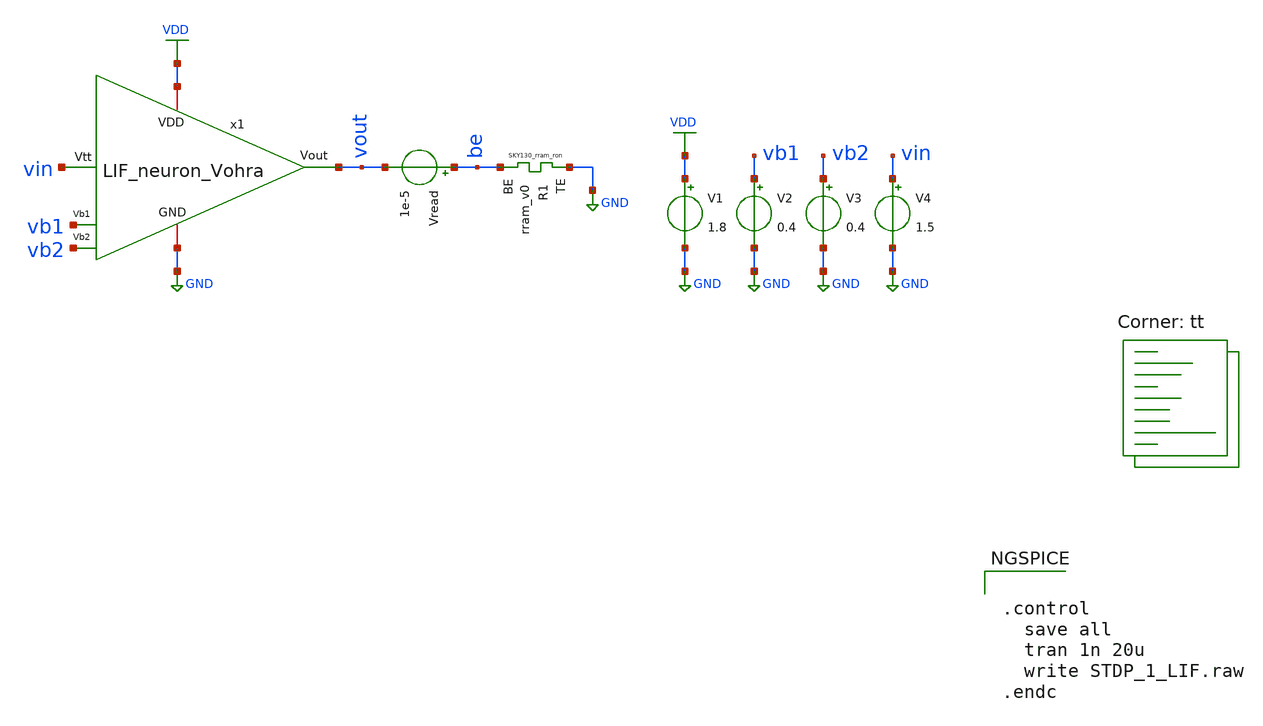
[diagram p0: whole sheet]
** sch_path: STDP/STDP_1_LIF.sch
**.subckt STDP_1_LIF
x1 VDD vout vb1 vin GND vb2 LIF_neuron_Vohra
V1 VDD GND 1.8
V4 vin GND 1.5
V2 vb1 GND 0.4
V3 vb2 GND 0.4
Vread be vout 1e-5
XR1 GND be rram_v0
**** begin user architecture code
.lib $::SKYWATER_MODELS/sky130.lib.spice tt

** opencircuitdesign pdks install
.inc $::SKYWATER_MODELS/rram_v0.spice



.control
  save all
  tran 1n 20u
  write STDP_1_LIF.raw
.endc


**** end user architecture code
**.ends

* expanding   symbol:  /home/ricardo/RATT_repos/Proyectos_xschem/LIF_neuron/LIF_neuron_Vohra.sym #
*+ of pins=6
** sym_path: LIF_neuron/LIF_neuron_Vohra.sym
** sch_path: LIF_neuron/LIF_neuron_Vohra.sch
.subckt LIF_neuron_Vohra VDD Vout Vb1 Vtt GND Vb2
*.ipin Vtt
*.iopin GND
*.ipin Vb1
*.ipin Vb2
*.iopin VDD
*.opin Vout
XM1 net3 Vtt GND GND sky130_fd_pr__nfet_01v8 L=1 W=0.6 nf=1 ad='int((nf+1)/2) * W/nf * 0.29' as='int((nf+2)/2) * W/nf * 0.29'
+ pd='2*int((nf+1)/2) * (W/nf + 0.29)' ps='2*int((nf+2)/2) * (W/nf + 0.29)' nrd='0.29 / W' nrs='0.29 / W'
+ sa=0 sb=0 sd=0 mult=1 m=1
XM3 net3 net3 VDD VDD sky130_fd_pr__pfet_01v8 L=1 W=0.6 nf=1 ad='int((nf+1)/2) * W/nf * 0.29' as='int((nf+2)/2) * W/nf * 0.29'
+ pd='2*int((nf+1)/2) * (W/nf + 0.29)' ps='2*int((nf+2)/2) * (W/nf + 0.29)' nrd='0.29 / W' nrs='0.29 / W'
+ sa=0 sb=0 sd=0 mult=1 m=1
XM13 net2 Vb1 GND GND sky130_fd_pr__nfet_01v8 L=0.5 W=5 nf=1 ad='int((nf+1)/2) * W/nf * 0.29' as='int((nf+2)/2) * W/nf * 0.29'
+ pd='2*int((nf+1)/2) * (W/nf + 0.29)' ps='2*int((nf+2)/2) * (W/nf + 0.29)' nrd='0.29 / W' nrs='0.29 / W'
+ sa=0 sb=0 sd=0 mult=1 m=1
XM12 rc net1 net2 GND sky130_fd_pr__nfet_01v8 L=1 W=1 nf=1 ad='int((nf+1)/2) * W/nf * 0.29' as='int((nf+2)/2) * W/nf * 0.29'
+ pd='2*int((nf+1)/2) * (W/nf + 0.29)' ps='2*int((nf+2)/2) * (W/nf + 0.29)' nrd='0.29 / W' nrs='0.29 / W'
+ sa=0 sb=0 sd=0 mult=1 m=1
XM11 rc net1 VDD VDD sky130_fd_pr__pfet_01v8 L=1 W=1 nf=1 ad='int((nf+1)/2) * W/nf * 0.29' as='int((nf+2)/2) * W/nf * 0.29'
+ pd='2*int((nf+1)/2) * (W/nf + 0.29)' ps='2*int((nf+2)/2) * (W/nf + 0.29)' nrd='0.29 / W' nrs='0.29 / W'
+ sa=0 sb=0 sd=0 mult=1 m=1
XC1 rc GND sky130_fd_pr__cap_mim_m3_1 W=21 L=1 MF=1 m=1
XM14 u rc GND GND sky130_fd_pr__nfet_01v8 L=4 W=1 nf=1 ad='int((nf+1)/2) * W/nf * 0.29' as='int((nf+2)/2) * W/nf * 0.29'
+ pd='2*int((nf+1)/2) * (W/nf + 0.29)' ps='2*int((nf+2)/2) * (W/nf + 0.29)' nrd='0.29 / W' nrs='0.29 / W'
+ sa=0 sb=0 sd=0 mult=1 m=1
XM4 u net3 VDD VDD sky130_fd_pr__pfet_01v8 L=1 W=1 nf=1 ad='int((nf+1)/2) * W/nf * 0.29' as='int((nf+2)/2) * W/nf * 0.29'
+ pd='2*int((nf+1)/2) * (W/nf + 0.29)' ps='2*int((nf+2)/2) * (W/nf + 0.29)' nrd='0.29 / W' nrs='0.29 / W'
+ sa=0 sb=0 sd=0 mult=1 m=1
XC2 u GND sky130_fd_pr__cap_mim_m3_1 W=10 L=1 MF=50 m=50
XM5 u Vb2 GND GND sky130_fd_pr__nfet_01v8 L=1 W=2 nf=1 ad='int((nf+1)/2) * W/nf * 0.29' as='int((nf+2)/2) * W/nf * 0.29'
+ pd='2*int((nf+1)/2) * (W/nf + 0.29)' ps='2*int((nf+2)/2) * (W/nf + 0.29)' nrd='0.29 / W' nrs='0.29 / W'
+ sa=0 sb=0 sd=0 mult=1 m=1
XM6 net4 Vout GND GND sky130_fd_pr__nfet_01v8 L=0.5 W=1 nf=1 ad='int((nf+1)/2) * W/nf * 0.29' as='int((nf+2)/2) * W/nf * 0.29'
+ pd='2*int((nf+1)/2) * (W/nf + 0.29)' ps='2*int((nf+2)/2) * (W/nf + 0.29)' nrd='0.29 / W' nrs='0.29 / W'
+ sa=0 sb=0 sd=0 mult=1 m=1
XM7 net1 u net4 GND sky130_fd_pr__nfet_01v8 L=1 W=1 nf=1 ad='int((nf+1)/2) * W/nf * 0.29' as='int((nf+2)/2) * W/nf * 0.29'
+ pd='2*int((nf+1)/2) * (W/nf + 0.29)' ps='2*int((nf+2)/2) * (W/nf + 0.29)' nrd='0.29 / W' nrs='0.29 / W'
+ sa=0 sb=0 sd=0 mult=1 m=1
XM8 net1 u VDD VDD sky130_fd_pr__pfet_01v8 L=1 W=1 nf=1 ad='int((nf+1)/2) * W/nf * 0.29' as='int((nf+2)/2) * W/nf * 0.29'
+ pd='2*int((nf+1)/2) * (W/nf + 0.29)' ps='2*int((nf+2)/2) * (W/nf + 0.29)' nrd='0.29 / W' nrs='0.29 / W'
+ sa=0 sb=0 sd=0 mult=1 m=1
XM9 Vout net1 net4 GND sky130_fd_pr__nfet_01v8 L=1 W=1 nf=1 ad='int((nf+1)/2) * W/nf * 0.29' as='int((nf+2)/2) * W/nf * 0.29'
+ pd='2*int((nf+1)/2) * (W/nf + 0.29)' ps='2*int((nf+2)/2) * (W/nf + 0.29)' nrd='0.29 / W' nrs='0.29 / W'
+ sa=0 sb=0 sd=0 mult=1 m=1
XM10 Vout net1 VDD VDD sky130_fd_pr__pfet_01v8 L=1 W=5 nf=1 ad='int((nf+1)/2) * W/nf * 0.29' as='int((nf+2)/2) * W/nf * 0.29'
+ pd='2*int((nf+1)/2) * (W/nf + 0.29)' ps='2*int((nf+2)/2) * (W/nf + 0.29)' nrd='0.29 / W' nrs='0.29 / W'
+ sa=0 sb=0 sd=0 mult=1 m=1
.ends

.GLOBAL GND
.GLOBAL VDD
.end
